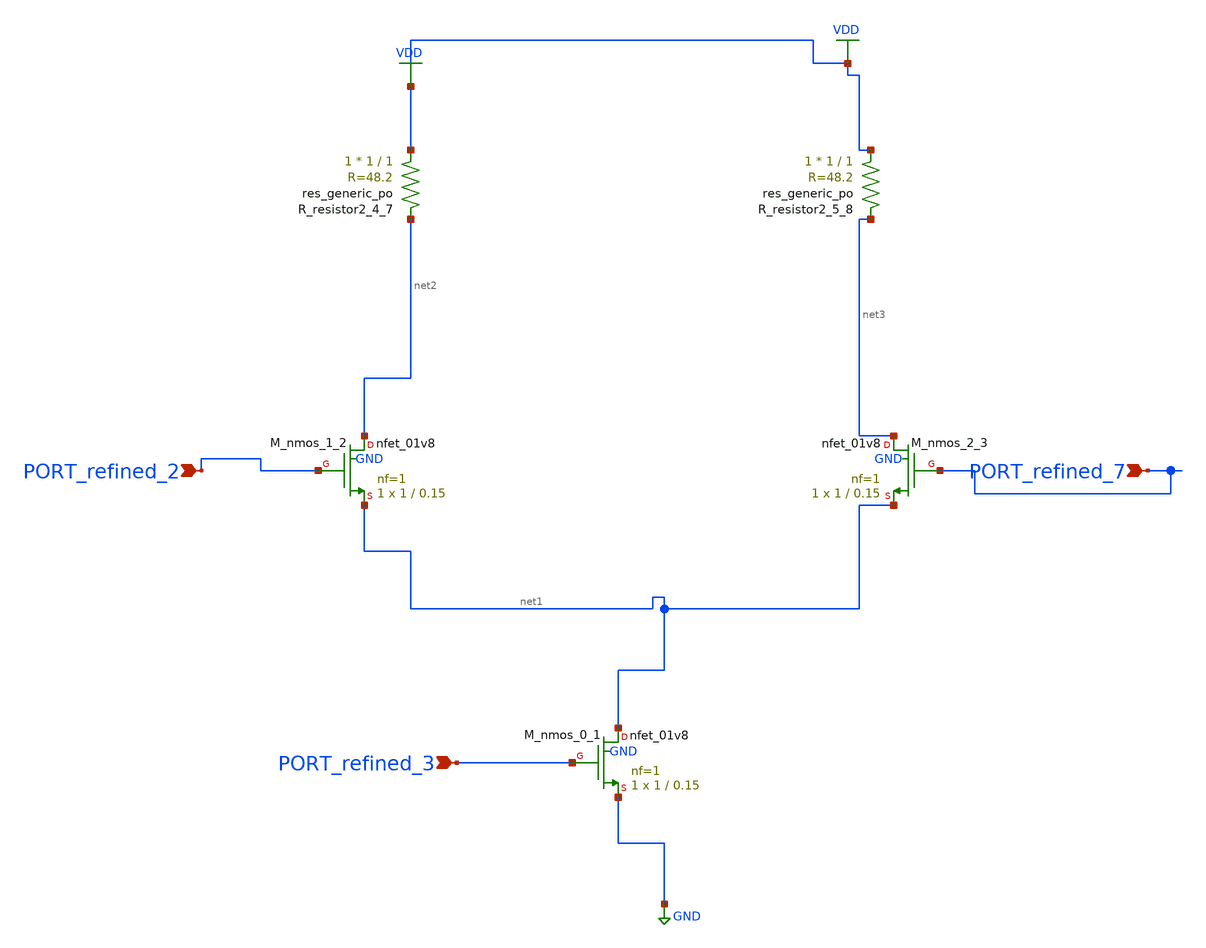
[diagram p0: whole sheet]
** sch_path: schematics/AMSNet/823.sch
**.subckt 823 PORT_refined_7 PORT_refined_2 PORT_refined_3
*.ipin PORT_refined_7
*.ipin PORT_refined_2
*.ipin PORT_refined_3
XM_nmos_0_1 net1 PORT_refined_3 GND GND sky130_fd_pr__nfet_01v8 L=0.15 W=1 nf=1 ad='int((1 + 1)/2) * 1 / 1 * 0.29'
+ as='int((1 + 2)/2) * 1 / 1 * 0.29' pd='2*int((1 + 1)/2) * (1 / 1 + 0.29)' ps='2*int((1 + 2)/2) * (1 / 1 + 0.29)'
+ nrd='0.29 / 1 ' nrs='0.29 / 1 ' sa=0 sb=0 sd=0 mult=1 m=1
XM_nmos_1_2 net2 PORT_refined_2 net1 GND sky130_fd_pr__nfet_01v8 L=0.15 W=1 nf=1 ad='int((1 + 1)/2) * 1 / 1 * 0.29'
+ as='int((1 + 2)/2) * 1 / 1 * 0.29' pd='2*int((1 + 1)/2) * (1 / 1 + 0.29)' ps='2*int((1 + 2)/2) * (1 / 1 + 0.29)'
+ nrd='0.29 / 1 ' nrs='0.29 / 1 ' sa=0 sb=0 sd=0 mult=1 m=1
XM_nmos_2_3 net3 PORT_refined_7 net1 GND sky130_fd_pr__nfet_01v8 L=0.15 W=1 nf=1 ad='int((1 + 1)/2) * 1 / 1 * 0.29'
+ as='int((1 + 2)/2) * 1 / 1 * 0.29' pd='2*int((1 + 1)/2) * (1 / 1 + 0.29)' ps='2*int((1 + 2)/2) * (1 / 1 + 0.29)'
+ nrd='0.29 / 1 ' nrs='0.29 / 1 ' sa=0 sb=0 sd=0 mult=1 m=1
XR_resistor2_4_7 VDD net2 sky130_fd_pr__res_generic_po W=1 L=1 m=1
XR_resistor2_5_8 VDD net3 sky130_fd_pr__res_generic_po W=1 L=1 m=1
**.ends
.GLOBAL GND
.GLOBAL VDD
.end
